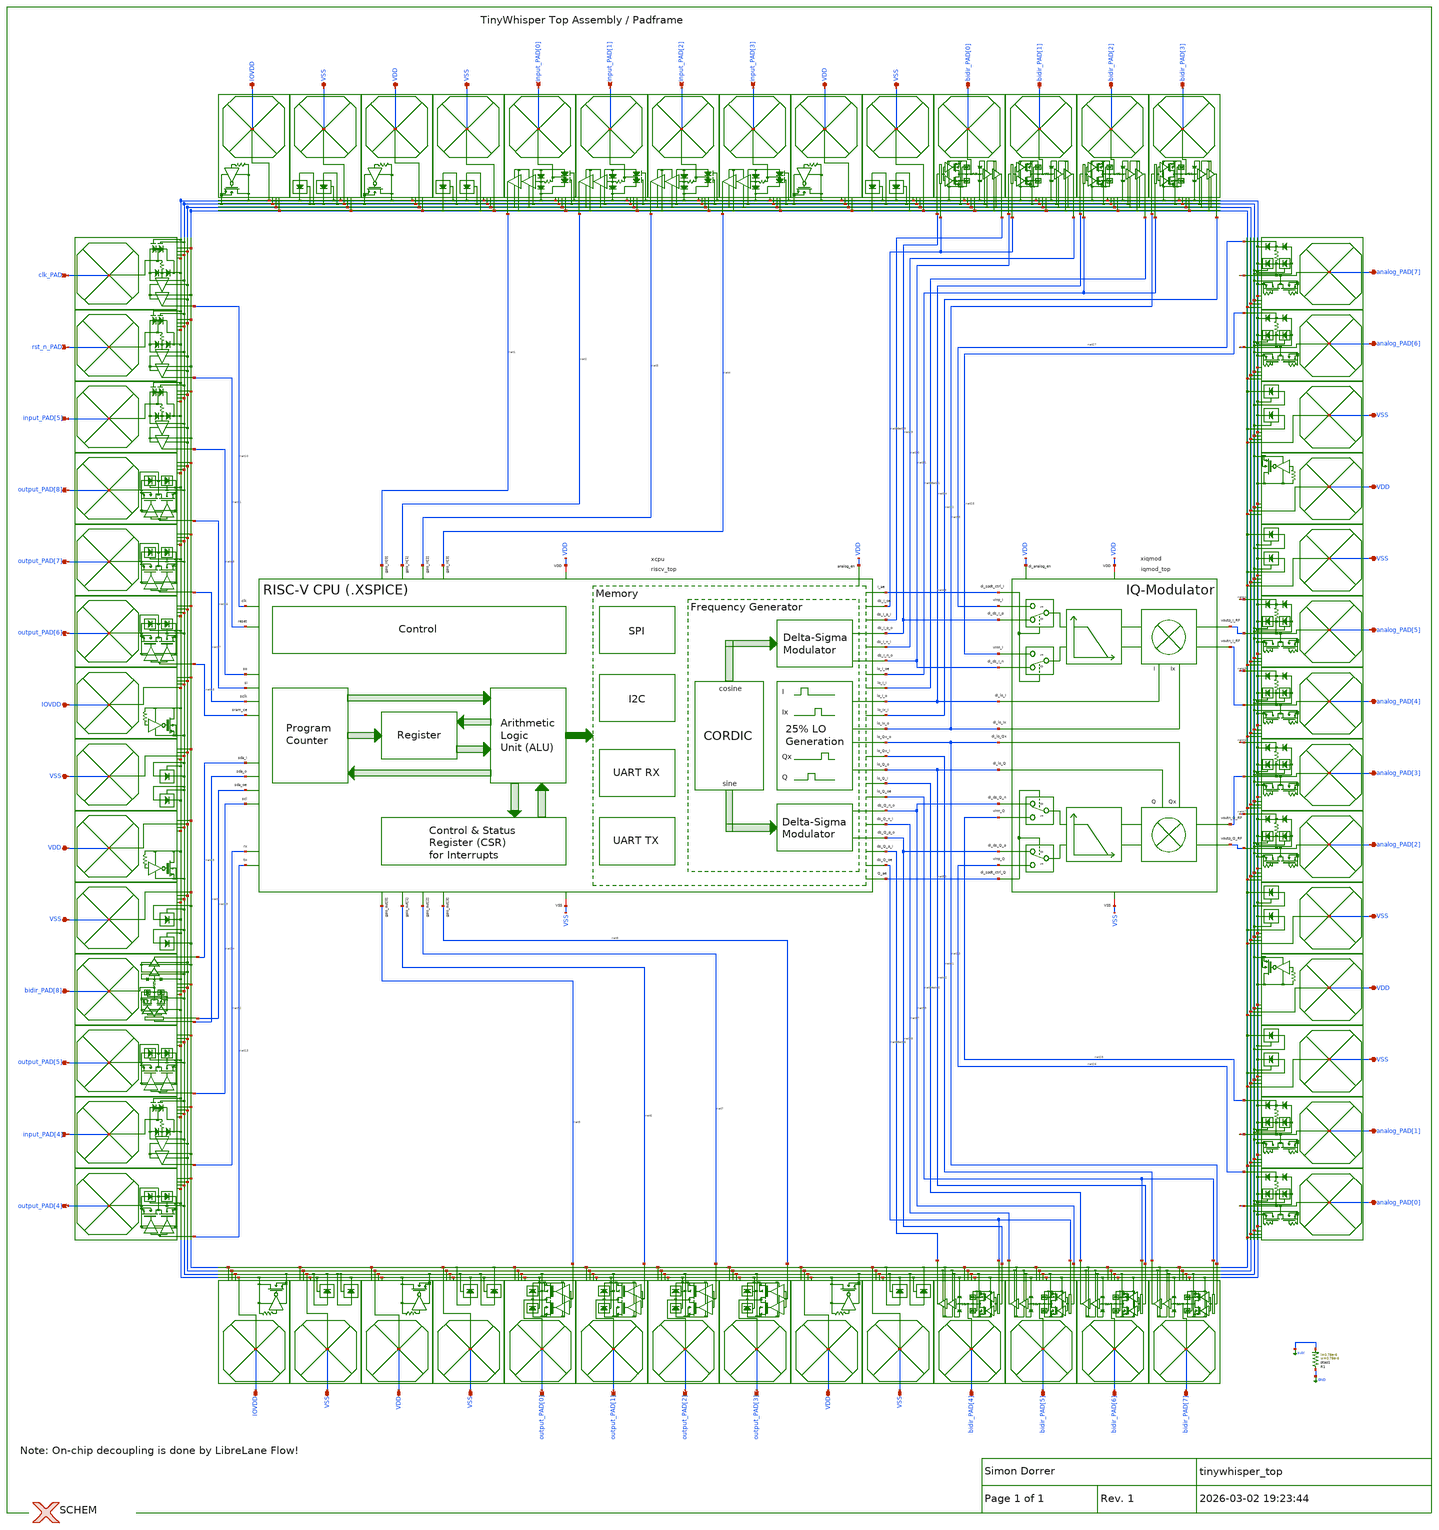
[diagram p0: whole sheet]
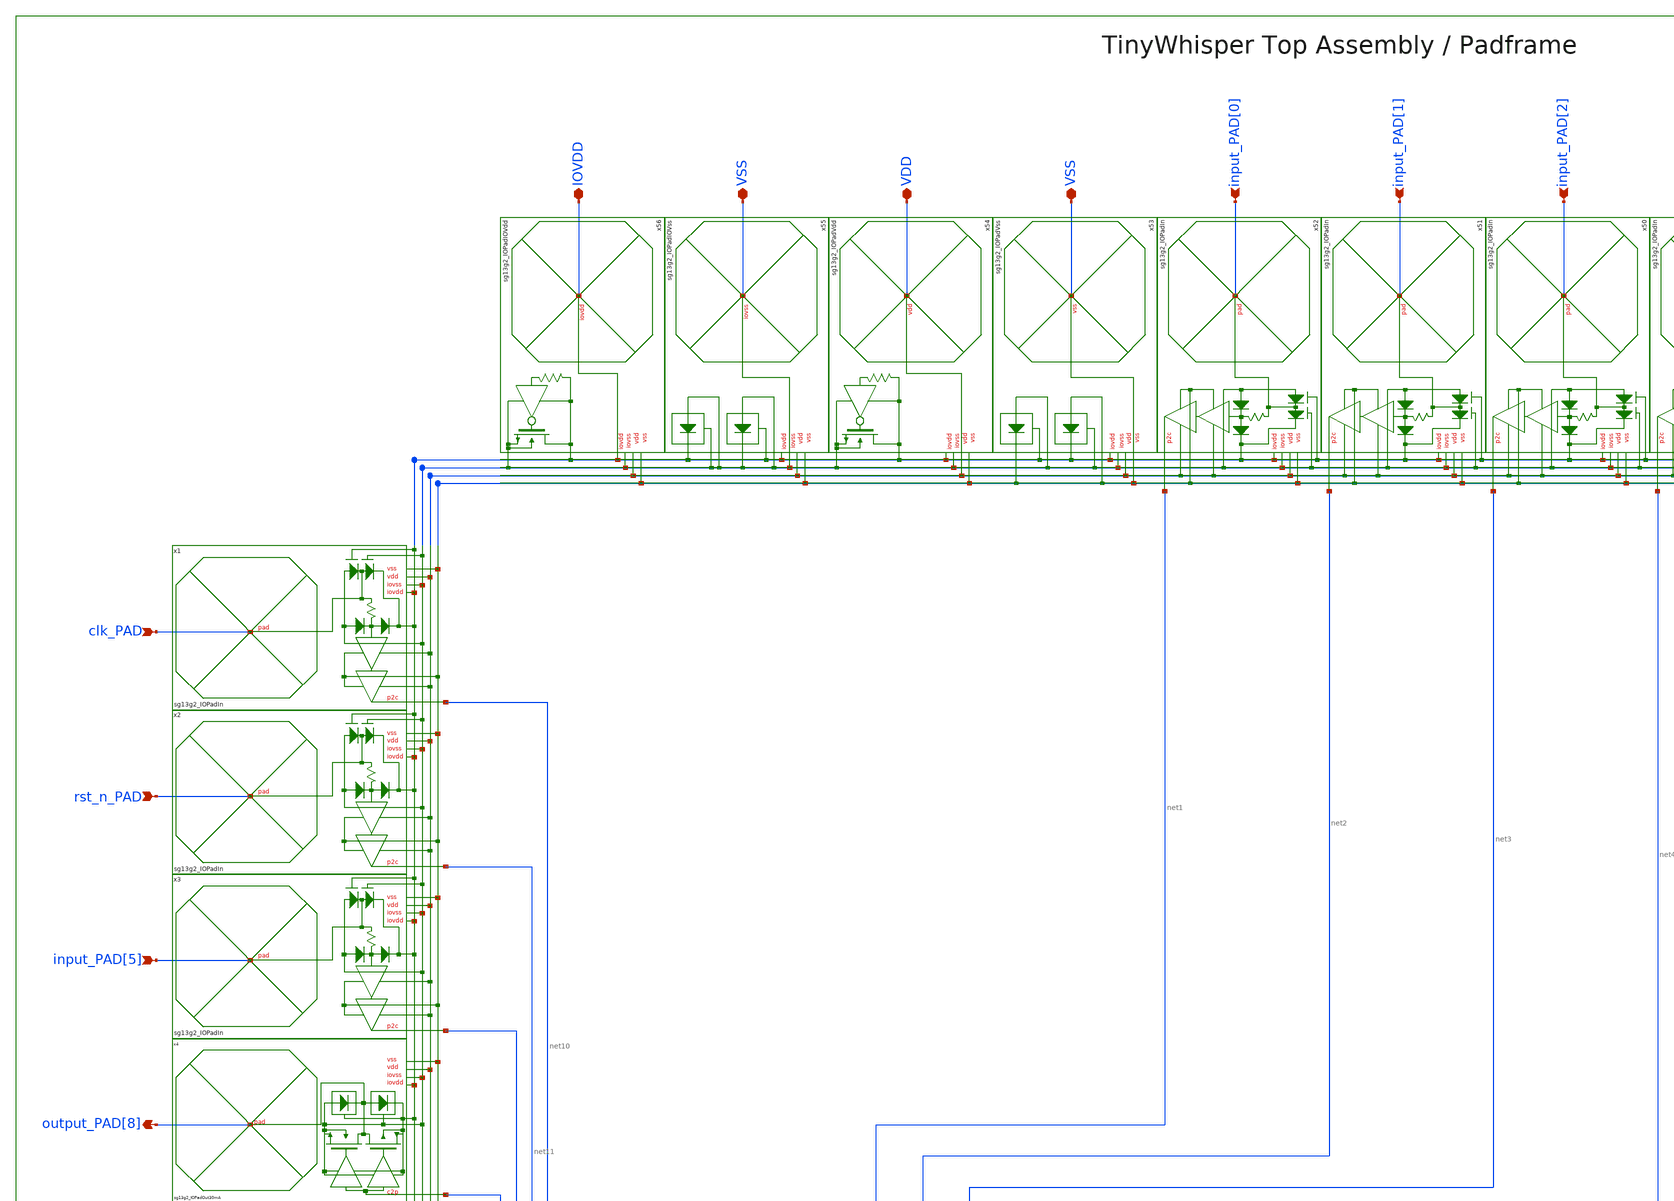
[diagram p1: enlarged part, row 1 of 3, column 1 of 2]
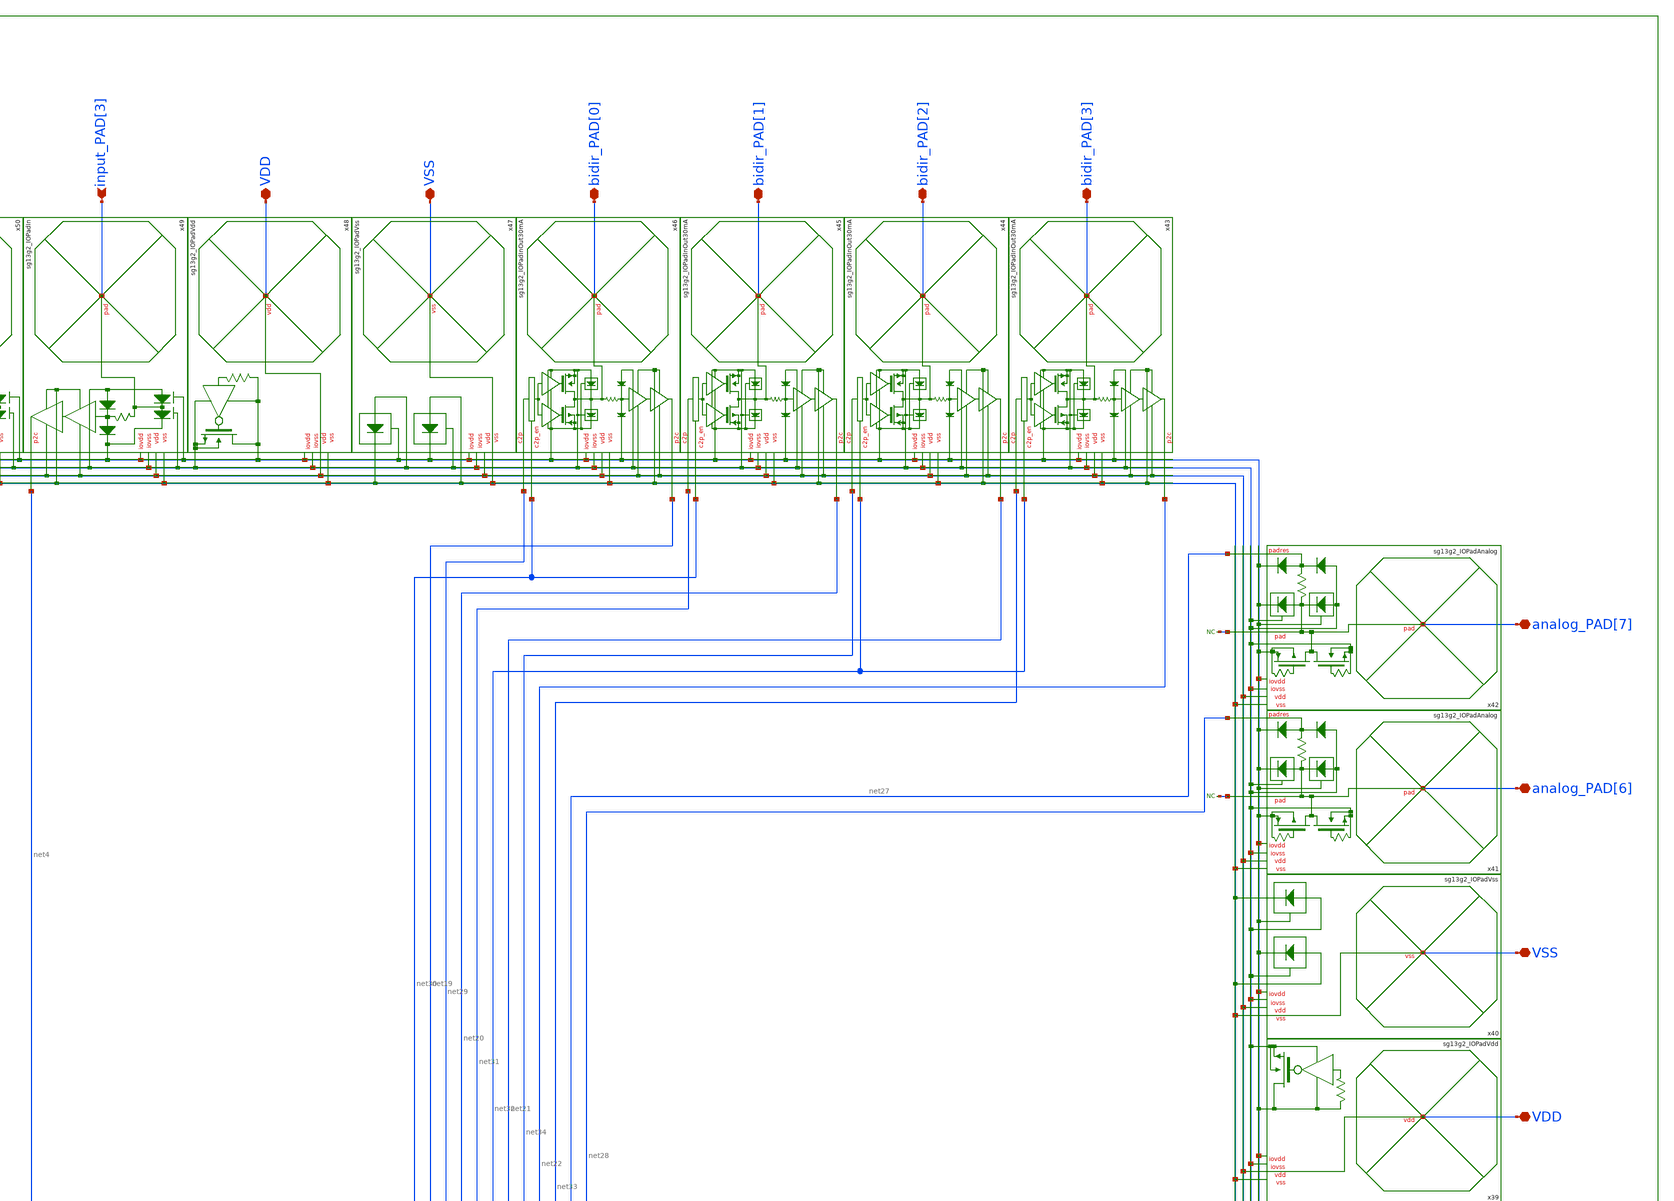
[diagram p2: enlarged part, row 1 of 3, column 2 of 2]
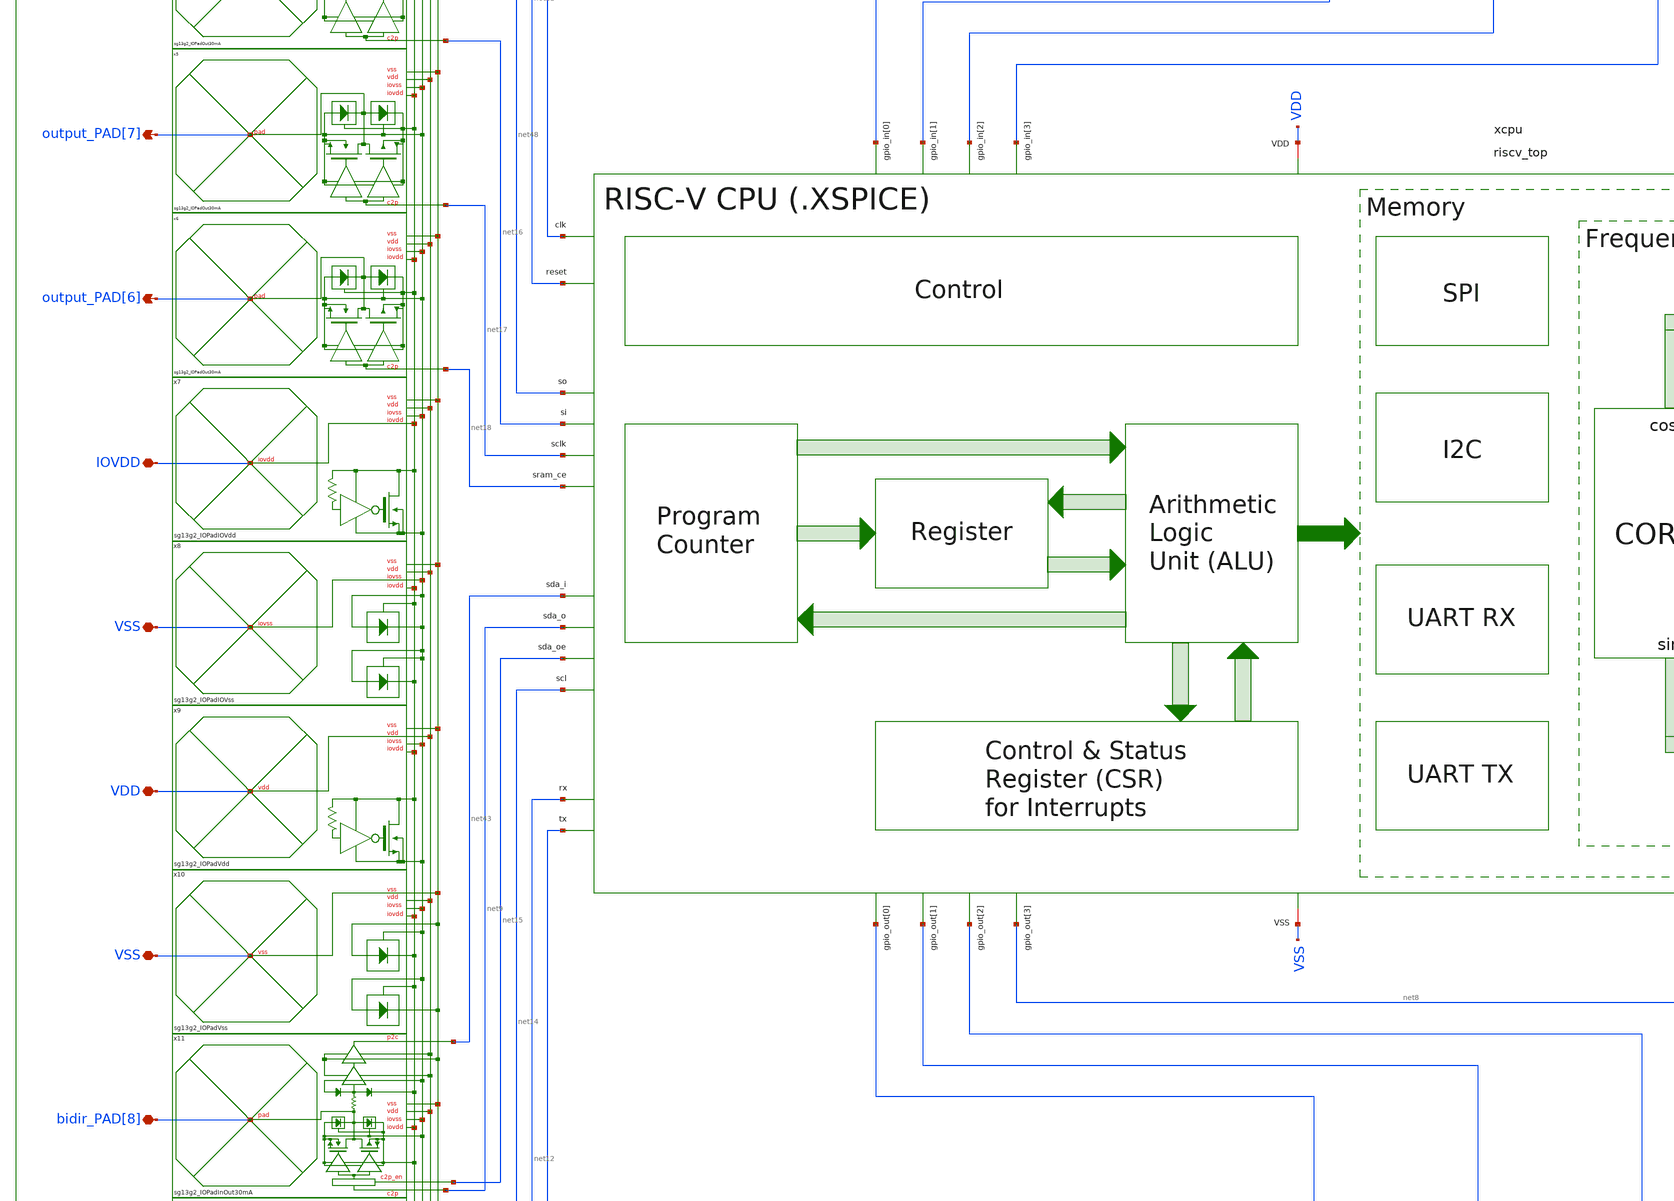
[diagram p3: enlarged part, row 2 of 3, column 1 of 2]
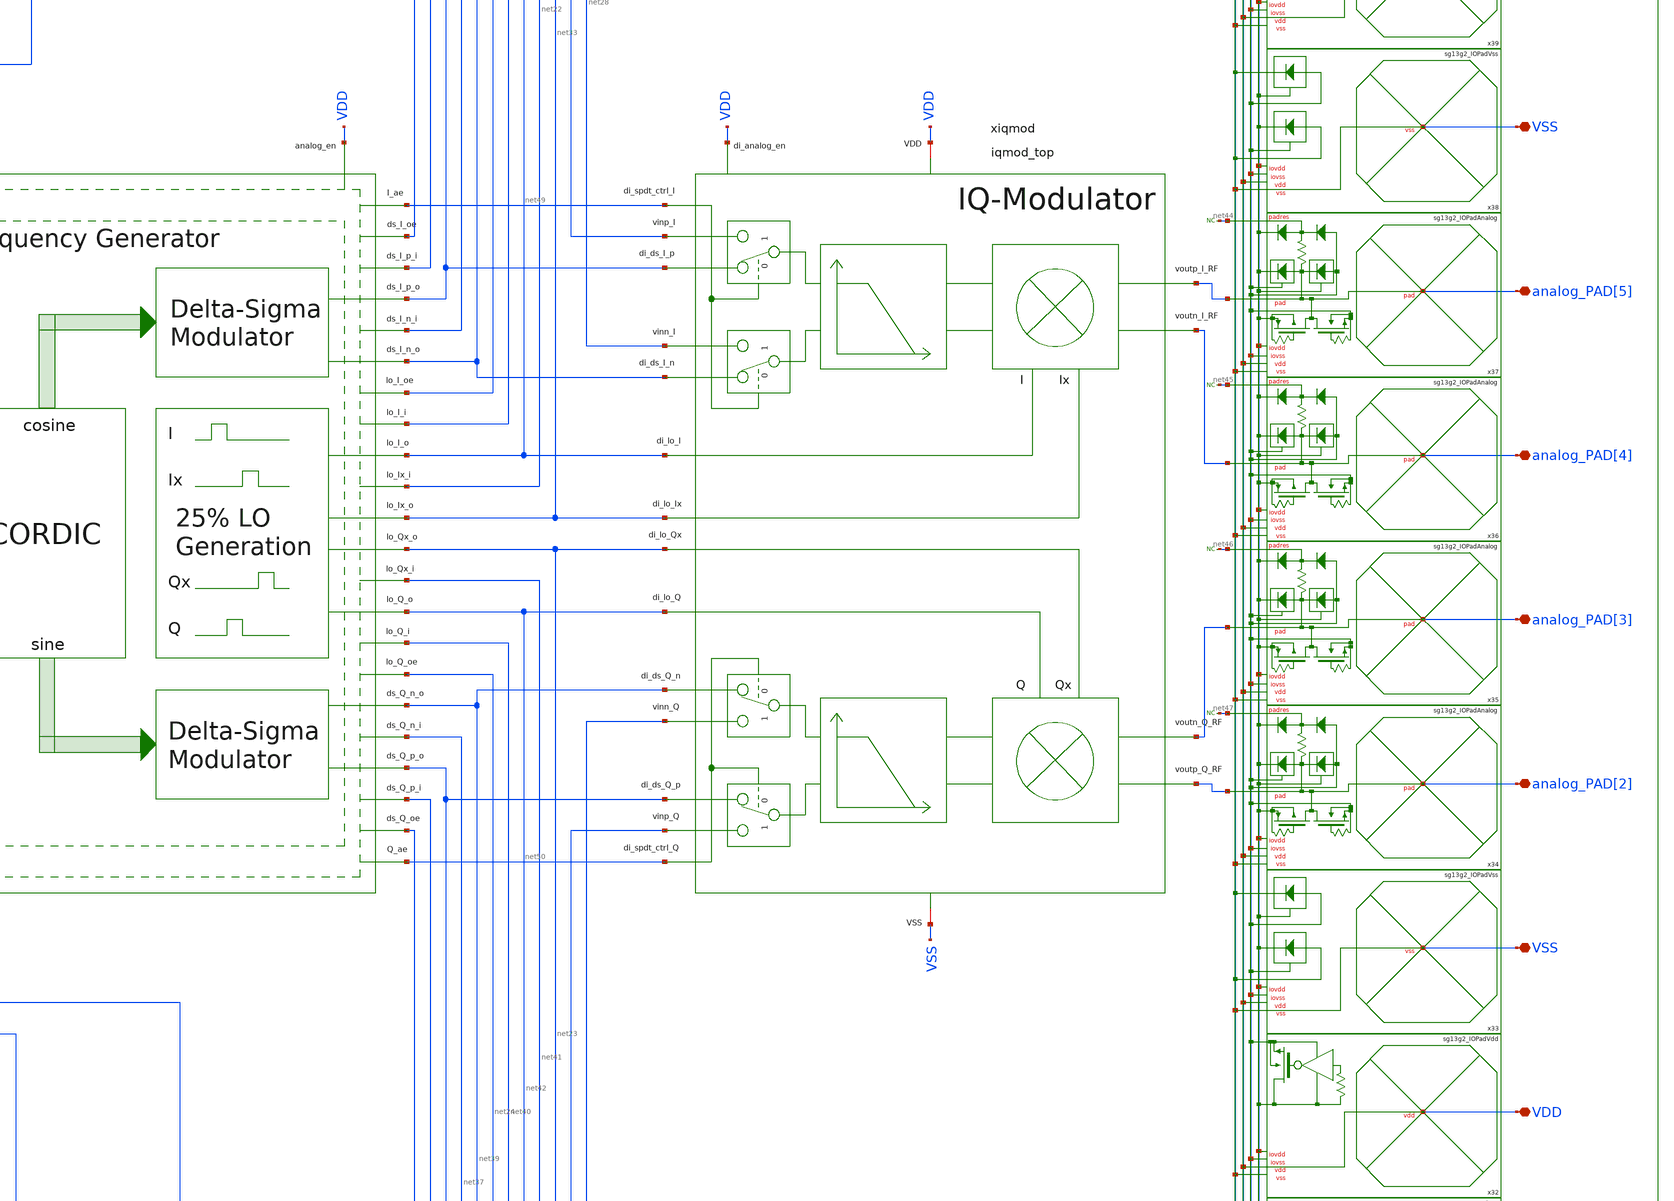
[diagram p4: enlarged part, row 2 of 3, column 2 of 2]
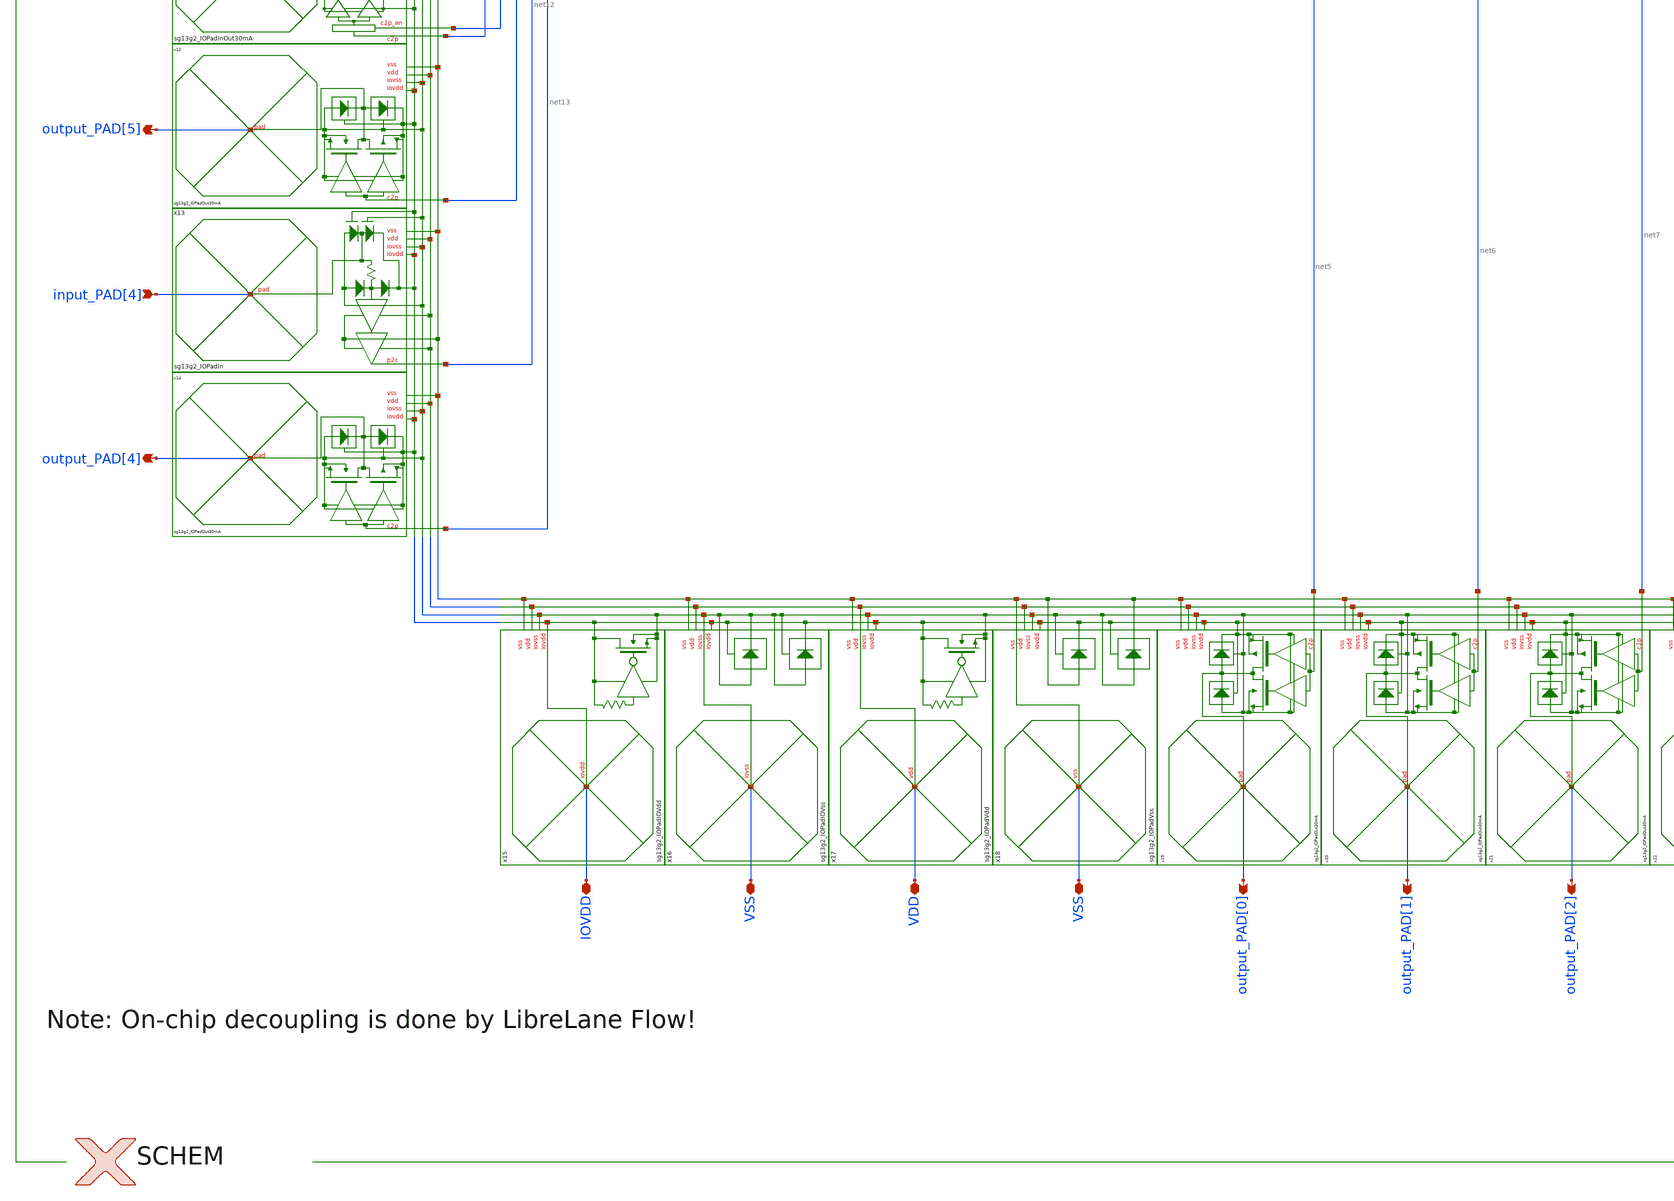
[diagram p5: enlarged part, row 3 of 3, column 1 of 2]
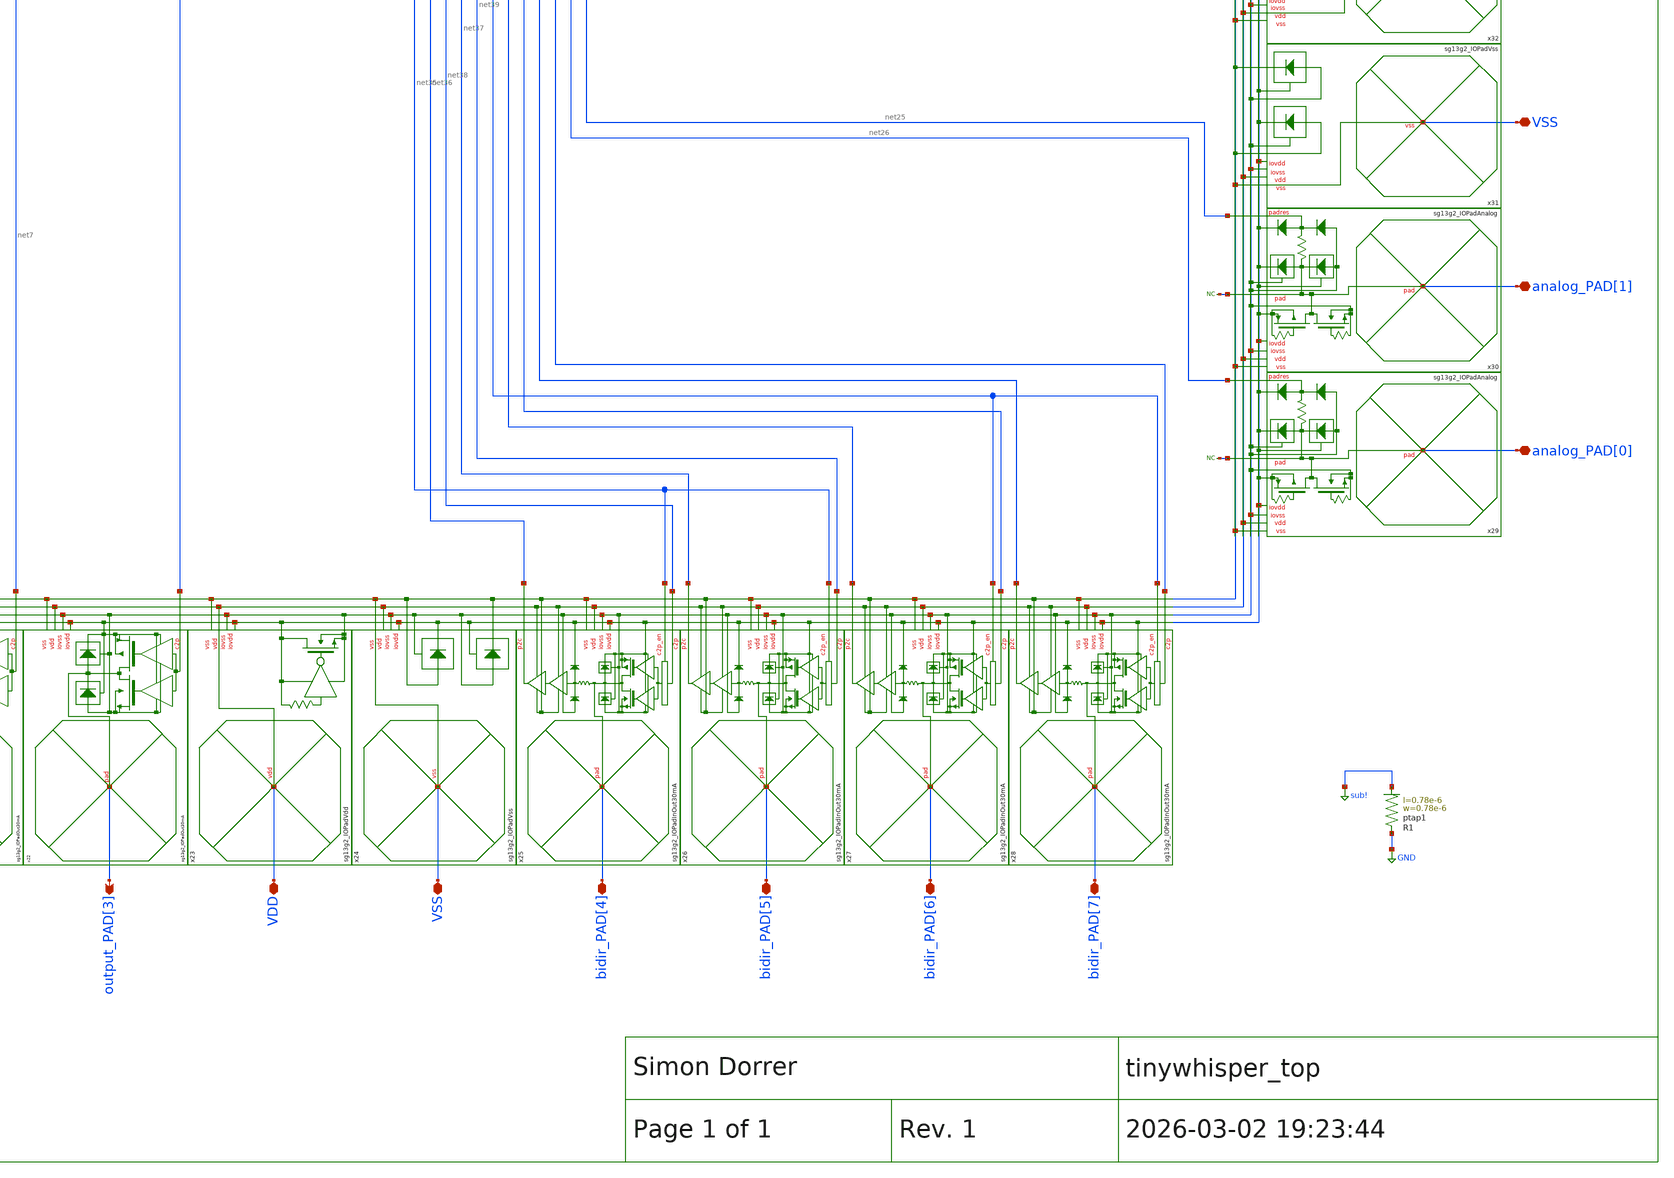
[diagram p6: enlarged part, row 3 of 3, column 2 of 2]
** sch_path: ihp130/xschem/tinywhisper_top.sch
**.subckt tinywhisper_top IOVDD VSS VDD VSS VDD VSS VDD VSS VSS clk_PAD rst_n_PAD input_PAD[5]
*+ input_PAD[4] output_PAD[4] output_PAD[8] output_PAD[7] output_PAD[6] output_PAD[5] input_PAD[3] input_PAD[2]
*+ input_PAD[1] input_PAD[0] output_PAD[3] output_PAD[2] output_PAD[1] output_PAD[0] analog_PAD[5] analog_PAD[4]
*+ analog_PAD[2] analog_PAD[3] analog_PAD[7] analog_PAD[6] analog_PAD[0] analog_PAD[1] VDD VSS VSS IOVDD VSS VDD VSS
*+ IOVDD VSS VDD VSS bidir_PAD[8] VDD VSS bidir_PAD[4] bidir_PAD[5] bidir_PAD[7] bidir_PAD[6] bidir_PAD[0]
*+ bidir_PAD[1] bidir_PAD[3] bidir_PAD[2]
*.iopin IOVDD
*.iopin VSS
*.iopin VDD
*.iopin VSS
*.iopin VDD
*.iopin VSS
*.iopin VDD
*.iopin VSS
*.iopin VSS
*.ipin clk_PAD
*.ipin rst_n_PAD
*.ipin input_PAD[5]
*.ipin input_PAD[4]
*.opin output_PAD[4]
*.opin output_PAD[8]
*.opin output_PAD[7]
*.opin output_PAD[6]
*.opin output_PAD[5]
*.ipin input_PAD[3]
*.ipin input_PAD[2]
*.ipin input_PAD[1]
*.ipin input_PAD[0]
*.opin output_PAD[3]
*.opin output_PAD[2]
*.opin output_PAD[1]
*.opin output_PAD[0]
*.iopin analog_PAD[5]
*.iopin analog_PAD[4]
*.iopin analog_PAD[2]
*.iopin analog_PAD[3]
*.iopin analog_PAD[7]
*.iopin analog_PAD[6]
*.iopin analog_PAD[0]
*.iopin analog_PAD[1]
*.iopin VDD
*.iopin VSS
*.iopin VSS
*.iopin IOVDD
*.iopin VSS
*.iopin VDD
*.iopin VSS
*.iopin IOVDD
*.iopin VSS
*.iopin VDD
*.iopin VSS
*.iopin bidir_PAD[8]
*.iopin VDD
*.iopin VSS
*.iopin bidir_PAD[4]
*.iopin bidir_PAD[5]
*.iopin bidir_PAD[7]
*.iopin bidir_PAD[6]
*.iopin bidir_PAD[0]
*.iopin bidir_PAD[1]
*.iopin bidir_PAD[3]
*.iopin bidir_PAD[2]
x1 VSS VDD VSS IOVDD net10 clk_PAD sg13g2_IOPadIn
x2 VSS VDD VSS IOVDD net11 rst_n_PAD sg13g2_IOPadIn
x3 VSS VDD VSS IOVDD net48 input_PAD[5] sg13g2_IOPadIn
x4 VSS VDD VSS IOVDD net16 output_PAD[8] sg13g2_IOPadOut30mA
x5 VSS VDD VSS IOVDD net17 output_PAD[7] sg13g2_IOPadOut30mA
x6 VSS VDD VSS IOVDD net18 output_PAD[6] sg13g2_IOPadOut30mA
x7 VSS VDD VSS IOVDD sg13g2_IOPadIOVdd
x8 VSS VDD VSS IOVDD sg13g2_IOPadIOVss
x9 VSS VDD VSS IOVDD sg13g2_IOPadVdd
x10 VSS VDD VSS IOVDD sg13g2_IOPadVss
x12 VSS VDD VSS IOVDD net14 output_PAD[5] sg13g2_IOPadOut30mA
x13 VSS VDD VSS IOVDD net12 input_PAD[4] sg13g2_IOPadIn
x14 VSS VDD VSS IOVDD net13 output_PAD[4] sg13g2_IOPadOut30mA
x15 VSS VDD VSS IOVDD sg13g2_IOPadIOVdd
x16 VSS VDD VSS IOVDD sg13g2_IOPadIOVss
x17 VSS VDD VSS IOVDD sg13g2_IOPadVdd
x18 VSS VDD VSS IOVDD sg13g2_IOPadVss
x19 VSS VDD VSS IOVDD net5 output_PAD[0] sg13g2_IOPadOut30mA
x20 VSS VDD VSS IOVDD net6 output_PAD[1] sg13g2_IOPadOut30mA
x21 VSS VDD VSS IOVDD net7 output_PAD[2] sg13g2_IOPadOut30mA
x22 VSS VDD VSS IOVDD net8 output_PAD[3] sg13g2_IOPadOut30mA
x23 VSS VDD VSS IOVDD sg13g2_IOPadVdd
x24 VSS VDD VSS IOVDD sg13g2_IOPadVss
x29 VSS VDD VSS IOVDD analog_PAD[0] net26 sg13g2_IOPadAnalog
x30 VSS VDD VSS IOVDD analog_PAD[1] net25 sg13g2_IOPadAnalog
x31 VSS VDD VSS IOVDD sg13g2_IOPadVss
x32 VSS VDD VSS IOVDD sg13g2_IOPadVdd
x33 VSS VDD VSS IOVDD sg13g2_IOPadVss
x35 VSS VDD VSS IOVDD analog_PAD[3] net46 sg13g2_IOPadAnalog
x36 VSS VDD VSS IOVDD analog_PAD[4] net45 sg13g2_IOPadAnalog
x37 VSS VDD VSS IOVDD analog_PAD[5] net44 sg13g2_IOPadAnalog
x38 VSS VDD VSS IOVDD sg13g2_IOPadVss
x39 VSS VDD VSS IOVDD sg13g2_IOPadVdd
x40 VSS VDD VSS IOVDD sg13g2_IOPadVss
x48 VSS VDD VSS IOVDD sg13g2_IOPadVdd
x47 VSS VDD VSS IOVDD sg13g2_IOPadVss
x41 VSS VDD VSS IOVDD analog_PAD[6] net28 sg13g2_IOPadAnalog
x42 VSS VDD VSS IOVDD analog_PAD[7] net27 sg13g2_IOPadAnalog
x49 VSS VDD VSS IOVDD net4 input_PAD[3] sg13g2_IOPadIn
x50 VSS VDD VSS IOVDD net3 input_PAD[2] sg13g2_IOPadIn
x51 VSS VDD VSS IOVDD net2 input_PAD[1] sg13g2_IOPadIn
x52 VSS VDD VSS IOVDD net1 input_PAD[0] sg13g2_IOPadIn
x56 VSS VDD VSS IOVDD sg13g2_IOPadIOVdd
x55 VSS VDD VSS IOVDD sg13g2_IOPadIOVss
x54 VSS VDD VSS IOVDD sg13g2_IOPadVdd
x53 VSS VDD VSS IOVDD sg13g2_IOPadVss
x11 VSS VDD VSS IOVDD net43 net9 net15 bidir_PAD[8] sg13g2_IOPadInOut30mA
x25 VSS VDD VSS IOVDD net36 net38 net35 bidir_PAD[4] sg13g2_IOPadInOut30mA
x26 VSS VDD VSS IOVDD net37 net39 net35 bidir_PAD[5] sg13g2_IOPadInOut30mA
x27 VSS VDD VSS IOVDD net40 net42 net24 bidir_PAD[6] sg13g2_IOPadInOut30mA
x28 VSS VDD VSS IOVDD net41 net23 net24 bidir_PAD[7] sg13g2_IOPadInOut30mA
x43 VSS VDD VSS IOVDD net22 net33 net32 bidir_PAD[3] sg13g2_IOPadInOut30mA
x44 VSS VDD VSS IOVDD net21 net34 net32 bidir_PAD[2] sg13g2_IOPadInOut30mA
x45 VSS VDD VSS IOVDD net20 net31 net30 bidir_PAD[1] sg13g2_IOPadInOut30mA
x46 VSS VDD VSS IOVDD net19 net29 net30 bidir_PAD[0] sg13g2_IOPadInOut30mA
x34 VSS VDD VSS IOVDD analog_PAD[2] net47 sg13g2_IOPadAnalog
* noconn analog_PAD[7]
* noconn analog_PAD[6]
* noconn #net44
* noconn #net45
* noconn #net46
* noconn #net47
* noconn analog_PAD[1]
* noconn analog_PAD[0]
XR1 GND sub! ptap1 R=262.8 w=0.78e-6 l=0.78e-6
xcpu VDD VSS net49 net50 net10 net20 net31 net30 net19 net29 net37 net39 net35 net36 net38 net21
+ net34 net32 net22 net33 net40 net42 net24 net41 net23 net11 net12 net14 net17 net43 net9 net15 net16
+ net48 net18 net13 net1 net2 net3 net4 net5 net6 net7 net8 VDD riscv_top
xiqmod net29 net49 net31 net39 net50 net38 net26 net25 net34 net33 analog_PAD[5] net27 net28 net42
+ net23 analog_PAD[4] analog_PAD[2] analog_PAD[3] VDD VSS VDD iqmod_top
**.ends
.GLOBAL sub!
.GLOBAL GND
.end
